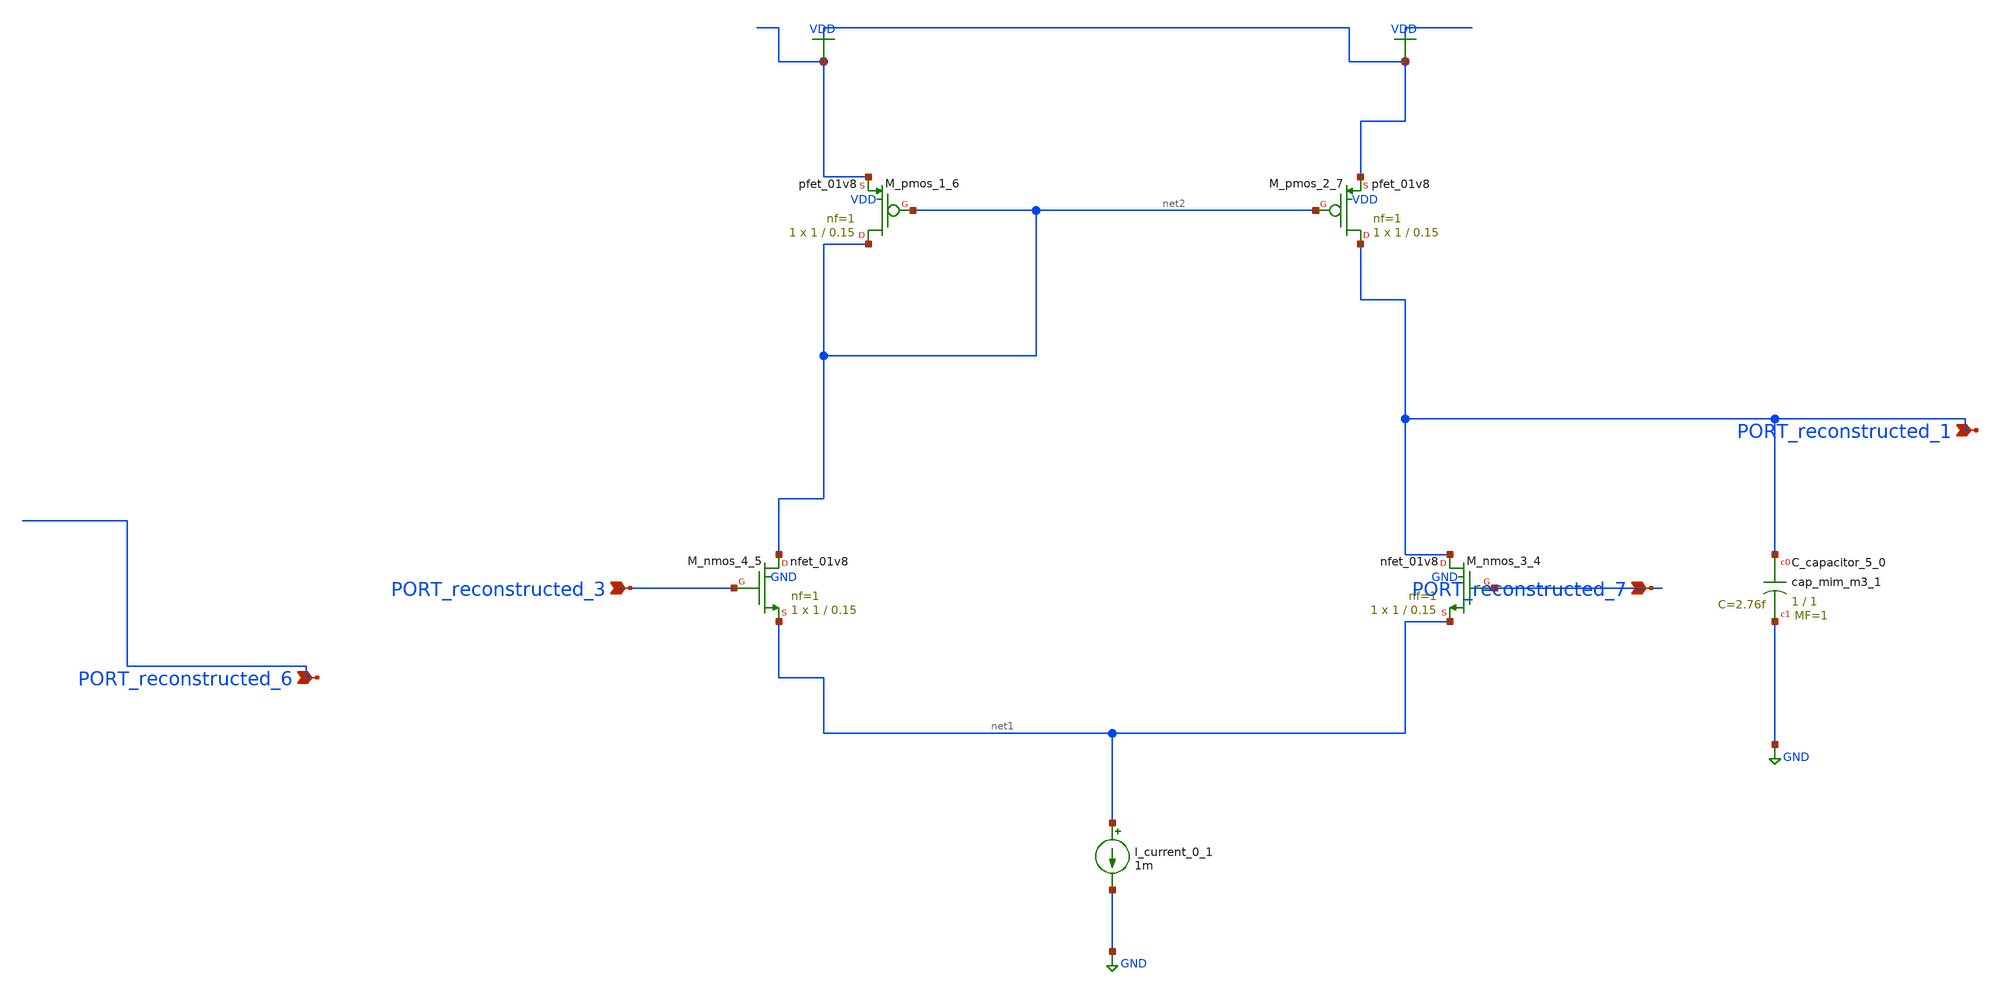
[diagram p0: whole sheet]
** sch_path: schematics/AMSNet/354.sch
**.subckt 354 PORT_reconstructed_3 PORT_reconstructed_6 PORT_reconstructed_1 PORT_reconstructed_7
*.ipin PORT_reconstructed_3
*.ipin PORT_reconstructed_6
*.ipin PORT_reconstructed_1
*.ipin PORT_reconstructed_7
XC_capacitor_5_0 PORT_reconstructed_1 GND sky130_fd_pr__cap_mim_m3_1 W=1 L=1 MF=1 m=1
I_current_0_1 net1 GND 1m
XM_nmos_3_4 PORT_reconstructed_1 PORT_reconstructed_7 net1 GND sky130_fd_pr__nfet_01v8 L=0.15 W=1 nf=1
+ ad='int((1 + 1)/2) * 1 / 1 * 0.29' as='int((1 + 2)/2) * 1 / 1 * 0.29' pd='2*int((1 + 1)/2) * (1 / 1 + 0.29)'
+ ps='2*int((1 + 2)/2) * (1 / 1 + 0.29)' nrd='0.29 / 1 ' nrs='0.29 / 1 ' sa=0 sb=0 sd=0 mult=1 m=1
XM_nmos_4_5 net2 PORT_reconstructed_3 net1 GND sky130_fd_pr__nfet_01v8 L=0.15 W=1 nf=1 ad='int((1 + 1)/2) * 1 / 1 * 0.29'
+ as='int((1 + 2)/2) * 1 / 1 * 0.29' pd='2*int((1 + 1)/2) * (1 / 1 + 0.29)' ps='2*int((1 + 2)/2) * (1 / 1 + 0.29)'
+ nrd='0.29 / 1 ' nrs='0.29 / 1 ' sa=0 sb=0 sd=0 mult=1 m=1
XM_pmos_1_6 net2 net2 VDD VDD sky130_fd_pr__pfet_01v8 L=0.15 W=1 nf=1 ad='int((1 + 1)/2) * 1 / 1 * 0.29'
+ as='int((1 + 2)/2) * 1 / 1 * 0.29' pd='2*int((1 + 1)/2) * (1 / 1 + 0.29)' ps='2*int((1 + 2)/2) * (1 / 1 + 0.29)'
+ nrd='0.29 / 1 ' nrs='0.29 / 1 ' sa=0 sb=0 sd=0 mult=1 m=1
XM_pmos_2_7 PORT_reconstructed_1 net2 VDD VDD sky130_fd_pr__pfet_01v8 L=0.15 W=1 nf=1 ad='int((1 + 1)/2) * 1 / 1 * 0.29'
+ as='int((1 + 2)/2) * 1 / 1 * 0.29' pd='2*int((1 + 1)/2) * (1 / 1 + 0.29)' ps='2*int((1 + 2)/2) * (1 / 1 + 0.29)'
+ nrd='0.29 / 1 ' nrs='0.29 / 1 ' sa=0 sb=0 sd=0 mult=1 m=1
**.ends
.GLOBAL GND
.GLOBAL VDD
.end
